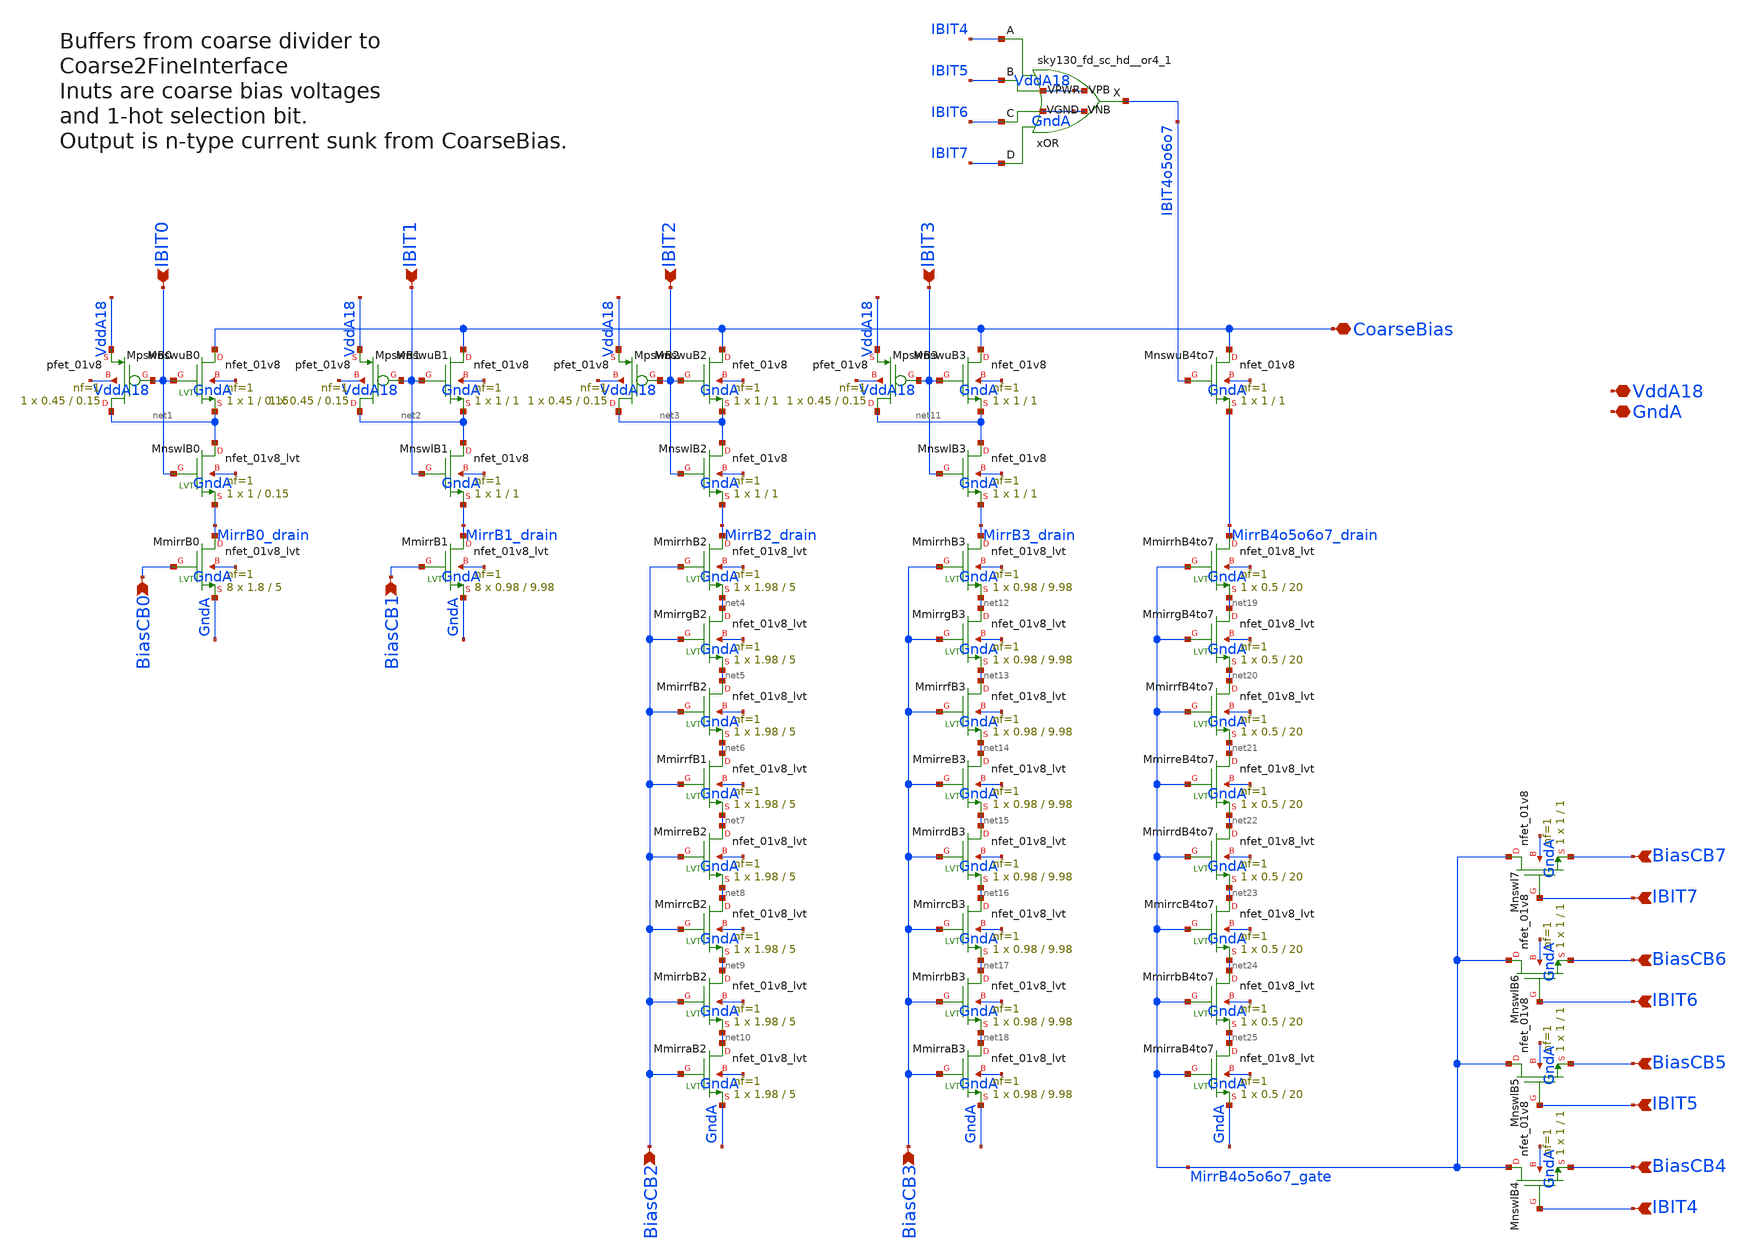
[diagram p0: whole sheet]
** sch_path: analog/xschem/BiasCoarseSel8to1.sch
**.subckt BiasCoarseSel8to1 IBIT0 BiasCB0 IBIT1 BiasCB1 IBIT2 BiasCB2 IBIT3 BiasCB3 BiasCB7 IBIT7
*+ BiasCB6 IBIT6 BiasCB5 IBIT5 BiasCB4 IBIT4 CoarseBias VddA18 GndA
*.ipin IBIT0
*.ipin BiasCB0
*.ipin IBIT1
*.ipin BiasCB1
*.ipin IBIT2
*.ipin BiasCB2
*.ipin IBIT3
*.ipin BiasCB3
*.ipin BiasCB7
*.ipin IBIT7
*.ipin BiasCB6
*.ipin IBIT6
*.ipin BiasCB5
*.ipin IBIT5
*.ipin BiasCB4
*.ipin IBIT4
*.iopin CoarseBias
*.iopin VddA18
*.iopin GndA
XMpswB0 net1 IBIT0 VddA18 VddA18 sky130_fd_pr__pfet_01v8 L=0.15 W=0.45 nf=1 ad='int((1 + 1)/2) * 0.45 / 1 * 0.29'
+ as='int((1 + 2)/2) * 0.45 / 1 * 0.29' pd='2*int((1 + 1)/2) * (0.45 / 1 + 0.29)' ps='2*int((1 + 2)/2) * (0.45 / 1 + 0.29)'
+ nrd='0.29 / 0.45 ' nrs='0.29 / 0.45 ' sa=0 sb=0 sd=0 mult=1 m=1
XMnswuB0 CoarseBias IBIT0 net1 GndA sky130_fd_pr__nfet_01v8 L=0.15 W=1 nf=1 ad='int((1 + 1)/2) * 1 / 1 * 0.29'
+ as='int((1 + 2)/2) * 1 / 1 * 0.29' pd='2*int((1 + 1)/2) * (1 / 1 + 0.29)' ps='2*int((1 + 2)/2) * (1 / 1 + 0.29)'
+ nrd='0.29 / 1 ' nrs='0.29 / 1 ' sa=0 sb=0 sd=0 mult=1 m=1
XMnswlB0 net1 IBIT0 MirrB0_drain GndA sky130_fd_pr__nfet_01v8_lvt L=0.15 W=1 nf=1 ad='int((1 + 1)/2) * 1 / 1 * 0.29'
+ as='int((1 + 2)/2) * 1 / 1 * 0.29' pd='2*int((1 + 1)/2) * (1 / 1 + 0.29)' ps='2*int((1 + 2)/2) * (1 / 1 + 0.29)'
+ nrd='0.29 / 1 ' nrs='0.29 / 1 ' sa=0 sb=0 sd=0 mult=1 m=1
XMmirrB0 MirrB0_drain BiasCB0 GndA GndA sky130_fd_pr__nfet_01v8_lvt L=5 W=1.8 nf=1 ad='int((1 + 1)/2) * 1.8 / 1 * 0.29'
+ as='int((1 + 2)/2) * 1.8 / 1 * 0.29' pd='2*int((1 + 1)/2) * (1.8 / 1 + 0.29)' ps='2*int((1 + 2)/2) * (1.8 / 1 + 0.29)'
+ nrd='0.29 / 1.8 ' nrs='0.29 / 1.8 ' sa=0 sb=0 sd=0 mult=8 m=8
XMpswB1 net2 IBIT1 VddA18 VddA18 sky130_fd_pr__pfet_01v8 L=0.15 W=0.45 nf=1 ad='int((1 + 1)/2) * 0.45 / 1 * 0.29'
+ as='int((1 + 2)/2) * 0.45 / 1 * 0.29' pd='2*int((1 + 1)/2) * (0.45 / 1 + 0.29)' ps='2*int((1 + 2)/2) * (0.45 / 1 + 0.29)'
+ nrd='0.29 / 0.45 ' nrs='0.29 / 0.45 ' sa=0 sb=0 sd=0 mult=1 m=1
XMnswuB1 CoarseBias IBIT1 net2 GndA sky130_fd_pr__nfet_01v8 L=1 W=1 nf=1 ad='int((1 + 1)/2) * 1 / 1 * 0.29'
+ as='int((1 + 2)/2) * 1 / 1 * 0.29' pd='2*int((1 + 1)/2) * (1 / 1 + 0.29)' ps='2*int((1 + 2)/2) * (1 / 1 + 0.29)'
+ nrd='0.29 / 1 ' nrs='0.29 / 1 ' sa=0 sb=0 sd=0 mult=1 m=1
XMnswlB1 net2 IBIT1 MirrB1_drain GndA sky130_fd_pr__nfet_01v8 L=1 W=1 nf=1 ad='int((1 + 1)/2) * 1 / 1 * 0.29'
+ as='int((1 + 2)/2) * 1 / 1 * 0.29' pd='2*int((1 + 1)/2) * (1 / 1 + 0.29)' ps='2*int((1 + 2)/2) * (1 / 1 + 0.29)'
+ nrd='0.29 / 1 ' nrs='0.29 / 1 ' sa=0 sb=0 sd=0 mult=1 m=1
XMmirrB1 MirrB1_drain BiasCB1 GndA GndA sky130_fd_pr__nfet_01v8_lvt L=9.98 W=0.98 nf=1 ad='int((1 + 1)/2) * 0.98 / 1 * 0.29'
+ as='int((1 + 2)/2) * 0.98 / 1 * 0.29' pd='2*int((1 + 1)/2) * (0.98 / 1 + 0.29)' ps='2*int((1 + 2)/2) * (0.98 / 1 + 0.29)'
+ nrd='0.29 / 0.98 ' nrs='0.29 / 0.98 ' sa=0 sb=0 sd=0 mult=8 m=8
XMpswB2 net3 IBIT2 VddA18 VddA18 sky130_fd_pr__pfet_01v8 L=0.15 W=0.45 nf=1 ad='int((1 + 1)/2) * 0.45 / 1 * 0.29'
+ as='int((1 + 2)/2) * 0.45 / 1 * 0.29' pd='2*int((1 + 1)/2) * (0.45 / 1 + 0.29)' ps='2*int((1 + 2)/2) * (0.45 / 1 + 0.29)'
+ nrd='0.29 / 0.45 ' nrs='0.29 / 0.45 ' sa=0 sb=0 sd=0 mult=1 m=1
XMnswuB2 CoarseBias IBIT2 net3 GndA sky130_fd_pr__nfet_01v8 L=1 W=1 nf=1 ad='int((1 + 1)/2) * 1 / 1 * 0.29'
+ as='int((1 + 2)/2) * 1 / 1 * 0.29' pd='2*int((1 + 1)/2) * (1 / 1 + 0.29)' ps='2*int((1 + 2)/2) * (1 / 1 + 0.29)'
+ nrd='0.29 / 1 ' nrs='0.29 / 1 ' sa=0 sb=0 sd=0 mult=1 m=1
XMnswlB2 net3 IBIT2 MirrB2_drain GndA sky130_fd_pr__nfet_01v8 L=1 W=1 nf=1 ad='int((1 + 1)/2) * 1 / 1 * 0.29'
+ as='int((1 + 2)/2) * 1 / 1 * 0.29' pd='2*int((1 + 1)/2) * (1 / 1 + 0.29)' ps='2*int((1 + 2)/2) * (1 / 1 + 0.29)'
+ nrd='0.29 / 1 ' nrs='0.29 / 1 ' sa=0 sb=0 sd=0 mult=1 m=1
XMmirrhB2 MirrB2_drain BiasCB2 net4 GndA sky130_fd_pr__nfet_01v8_lvt L=5 W=1.98 nf=1 ad='int((1 + 1)/2) * 1.98 / 1 * 0.29'
+ as='int((1 + 2)/2) * 1.98 / 1 * 0.29' pd='2*int((1 + 1)/2) * (1.98 / 1 + 0.29)' ps='2*int((1 + 2)/2) * (1.98 / 1 + 0.29)'
+ nrd='0.29 / 1.98 ' nrs='0.29 / 1.98 ' sa=0 sb=0 sd=0 mult=1 m=1
XMmirrgB2 net4 BiasCB2 net5 GndA sky130_fd_pr__nfet_01v8_lvt L=5 W=1.98 nf=1 ad='int((1 + 1)/2) * 1.98 / 1 * 0.29'
+ as='int((1 + 2)/2) * 1.98 / 1 * 0.29' pd='2*int((1 + 1)/2) * (1.98 / 1 + 0.29)' ps='2*int((1 + 2)/2) * (1.98 / 1 + 0.29)'
+ nrd='0.29 / 1.98 ' nrs='0.29 / 1.98 ' sa=0 sb=0 sd=0 mult=1 m=1
XMmirrfB2 net5 BiasCB2 net6 GndA sky130_fd_pr__nfet_01v8_lvt L=5 W=1.98 nf=1 ad='int((1 + 1)/2) * 1.98 / 1 * 0.29'
+ as='int((1 + 2)/2) * 1.98 / 1 * 0.29' pd='2*int((1 + 1)/2) * (1.98 / 1 + 0.29)' ps='2*int((1 + 2)/2) * (1.98 / 1 + 0.29)'
+ nrd='0.29 / 1.98 ' nrs='0.29 / 1.98 ' sa=0 sb=0 sd=0 mult=1 m=1
XMmirrfB1 net6 BiasCB2 net7 GndA sky130_fd_pr__nfet_01v8_lvt L=5 W=1.98 nf=1 ad='int((1 + 1)/2) * 1.98 / 1 * 0.29'
+ as='int((1 + 2)/2) * 1.98 / 1 * 0.29' pd='2*int((1 + 1)/2) * (1.98 / 1 + 0.29)' ps='2*int((1 + 2)/2) * (1.98 / 1 + 0.29)'
+ nrd='0.29 / 1.98 ' nrs='0.29 / 1.98 ' sa=0 sb=0 sd=0 mult=1 m=1
XMmirreB2 net7 BiasCB2 net8 GndA sky130_fd_pr__nfet_01v8_lvt L=5 W=1.98 nf=1 ad='int((1 + 1)/2) * 1.98 / 1 * 0.29'
+ as='int((1 + 2)/2) * 1.98 / 1 * 0.29' pd='2*int((1 + 1)/2) * (1.98 / 1 + 0.29)' ps='2*int((1 + 2)/2) * (1.98 / 1 + 0.29)'
+ nrd='0.29 / 1.98 ' nrs='0.29 / 1.98 ' sa=0 sb=0 sd=0 mult=1 m=1
XMmirrcB2 net8 BiasCB2 net9 GndA sky130_fd_pr__nfet_01v8_lvt L=5 W=1.98 nf=1 ad='int((1 + 1)/2) * 1.98 / 1 * 0.29'
+ as='int((1 + 2)/2) * 1.98 / 1 * 0.29' pd='2*int((1 + 1)/2) * (1.98 / 1 + 0.29)' ps='2*int((1 + 2)/2) * (1.98 / 1 + 0.29)'
+ nrd='0.29 / 1.98 ' nrs='0.29 / 1.98 ' sa=0 sb=0 sd=0 mult=1 m=1
XMmirrbB2 net9 BiasCB2 net10 GndA sky130_fd_pr__nfet_01v8_lvt L=5 W=1.98 nf=1 ad='int((1 + 1)/2) * 1.98 / 1 * 0.29'
+ as='int((1 + 2)/2) * 1.98 / 1 * 0.29' pd='2*int((1 + 1)/2) * (1.98 / 1 + 0.29)' ps='2*int((1 + 2)/2) * (1.98 / 1 + 0.29)'
+ nrd='0.29 / 1.98 ' nrs='0.29 / 1.98 ' sa=0 sb=0 sd=0 mult=1 m=1
XMmirraB2 net10 BiasCB2 GndA GndA sky130_fd_pr__nfet_01v8_lvt L=5 W=1.98 nf=1 ad='int((1 + 1)/2) * 1.98 / 1 * 0.29'
+ as='int((1 + 2)/2) * 1.98 / 1 * 0.29' pd='2*int((1 + 1)/2) * (1.98 / 1 + 0.29)' ps='2*int((1 + 2)/2) * (1.98 / 1 + 0.29)'
+ nrd='0.29 / 1.98 ' nrs='0.29 / 1.98 ' sa=0 sb=0 sd=0 mult=1 m=1
XMpswB3 net11 IBIT3 VddA18 VddA18 sky130_fd_pr__pfet_01v8 L=0.15 W=0.45 nf=1 ad='int((1 + 1)/2) * 0.45 / 1 * 0.29'
+ as='int((1 + 2)/2) * 0.45 / 1 * 0.29' pd='2*int((1 + 1)/2) * (0.45 / 1 + 0.29)' ps='2*int((1 + 2)/2) * (0.45 / 1 + 0.29)'
+ nrd='0.29 / 0.45 ' nrs='0.29 / 0.45 ' sa=0 sb=0 sd=0 mult=1 m=1
XMnswuB3 CoarseBias IBIT3 net11 GndA sky130_fd_pr__nfet_01v8 L=1 W=1 nf=1 ad='int((1 + 1)/2) * 1 / 1 * 0.29'
+ as='int((1 + 2)/2) * 1 / 1 * 0.29' pd='2*int((1 + 1)/2) * (1 / 1 + 0.29)' ps='2*int((1 + 2)/2) * (1 / 1 + 0.29)'
+ nrd='0.29 / 1 ' nrs='0.29 / 1 ' sa=0 sb=0 sd=0 mult=1 m=1
XMnswlB3 net11 IBIT3 MirrB3_drain GndA sky130_fd_pr__nfet_01v8 L=1 W=1 nf=1 ad='int((1 + 1)/2) * 1 / 1 * 0.29'
+ as='int((1 + 2)/2) * 1 / 1 * 0.29' pd='2*int((1 + 1)/2) * (1 / 1 + 0.29)' ps='2*int((1 + 2)/2) * (1 / 1 + 0.29)'
+ nrd='0.29 / 1 ' nrs='0.29 / 1 ' sa=0 sb=0 sd=0 mult=1 m=1
XMmirrhB3 MirrB3_drain BiasCB3 net12 GndA sky130_fd_pr__nfet_01v8_lvt L=9.98 W=0.98 nf=1 ad='int((1 + 1)/2) * 0.98 / 1 * 0.29'
+ as='int((1 + 2)/2) * 0.98 / 1 * 0.29' pd='2*int((1 + 1)/2) * (0.98 / 1 + 0.29)' ps='2*int((1 + 2)/2) * (0.98 / 1 + 0.29)'
+ nrd='0.29 / 0.98 ' nrs='0.29 / 0.98 ' sa=0 sb=0 sd=0 mult=1 m=1
XMmirrgB3 net12 BiasCB3 net13 GndA sky130_fd_pr__nfet_01v8_lvt L=9.98 W=0.98 nf=1 ad='int((1 + 1)/2) * 0.98 / 1 * 0.29'
+ as='int((1 + 2)/2) * 0.98 / 1 * 0.29' pd='2*int((1 + 1)/2) * (0.98 / 1 + 0.29)' ps='2*int((1 + 2)/2) * (0.98 / 1 + 0.29)'
+ nrd='0.29 / 0.98 ' nrs='0.29 / 0.98 ' sa=0 sb=0 sd=0 mult=1 m=1
XMmirrfB3 net13 BiasCB3 net14 GndA sky130_fd_pr__nfet_01v8_lvt L=9.98 W=0.98 nf=1 ad='int((1 + 1)/2) * 0.98 / 1 * 0.29'
+ as='int((1 + 2)/2) * 0.98 / 1 * 0.29' pd='2*int((1 + 1)/2) * (0.98 / 1 + 0.29)' ps='2*int((1 + 2)/2) * (0.98 / 1 + 0.29)'
+ nrd='0.29 / 0.98 ' nrs='0.29 / 0.98 ' sa=0 sb=0 sd=0 mult=1 m=1
XMmirreB3 net14 BiasCB3 net15 GndA sky130_fd_pr__nfet_01v8_lvt L=9.98 W=0.98 nf=1 ad='int((1 + 1)/2) * 0.98 / 1 * 0.29'
+ as='int((1 + 2)/2) * 0.98 / 1 * 0.29' pd='2*int((1 + 1)/2) * (0.98 / 1 + 0.29)' ps='2*int((1 + 2)/2) * (0.98 / 1 + 0.29)'
+ nrd='0.29 / 0.98 ' nrs='0.29 / 0.98 ' sa=0 sb=0 sd=0 mult=1 m=1
XMmirrdB3 net15 BiasCB3 net16 GndA sky130_fd_pr__nfet_01v8_lvt L=9.98 W=0.98 nf=1 ad='int((1 + 1)/2) * 0.98 / 1 * 0.29'
+ as='int((1 + 2)/2) * 0.98 / 1 * 0.29' pd='2*int((1 + 1)/2) * (0.98 / 1 + 0.29)' ps='2*int((1 + 2)/2) * (0.98 / 1 + 0.29)'
+ nrd='0.29 / 0.98 ' nrs='0.29 / 0.98 ' sa=0 sb=0 sd=0 mult=1 m=1
XMmirrcB3 net16 BiasCB3 net17 GndA sky130_fd_pr__nfet_01v8_lvt L=9.98 W=0.98 nf=1 ad='int((1 + 1)/2) * 0.98 / 1 * 0.29'
+ as='int((1 + 2)/2) * 0.98 / 1 * 0.29' pd='2*int((1 + 1)/2) * (0.98 / 1 + 0.29)' ps='2*int((1 + 2)/2) * (0.98 / 1 + 0.29)'
+ nrd='0.29 / 0.98 ' nrs='0.29 / 0.98 ' sa=0 sb=0 sd=0 mult=1 m=1
XMmirrbB3 net17 BiasCB3 net18 GndA sky130_fd_pr__nfet_01v8_lvt L=9.98 W=0.98 nf=1 ad='int((1 + 1)/2) * 0.98 / 1 * 0.29'
+ as='int((1 + 2)/2) * 0.98 / 1 * 0.29' pd='2*int((1 + 1)/2) * (0.98 / 1 + 0.29)' ps='2*int((1 + 2)/2) * (0.98 / 1 + 0.29)'
+ nrd='0.29 / 0.98 ' nrs='0.29 / 0.98 ' sa=0 sb=0 sd=0 mult=1 m=1
XMmirraB3 net18 BiasCB3 GndA GndA sky130_fd_pr__nfet_01v8_lvt L=9.98 W=0.98 nf=1 ad='int((1 + 1)/2) * 0.98 / 1 * 0.29'
+ as='int((1 + 2)/2) * 0.98 / 1 * 0.29' pd='2*int((1 + 1)/2) * (0.98 / 1 + 0.29)' ps='2*int((1 + 2)/2) * (0.98 / 1 + 0.29)'
+ nrd='0.29 / 0.98 ' nrs='0.29 / 0.98 ' sa=0 sb=0 sd=0 mult=1 m=1
XMnswuB4to7 CoarseBias IBIT4o5o6o7 MirrB4o5o6o7_drain GndA sky130_fd_pr__nfet_01v8 L=1 W=1 nf=1 ad='int((1 + 1)/2) * 1 / 1 * 0.29'
+ as='int((1 + 2)/2) * 1 / 1 * 0.29' pd='2*int((1 + 1)/2) * (1 / 1 + 0.29)' ps='2*int((1 + 2)/2) * (1 / 1 + 0.29)'
+ nrd='0.29 / 1 ' nrs='0.29 / 1 ' sa=0 sb=0 sd=0 mult=1 m=1
XMmirrhB4to7 MirrB4o5o6o7_drain MirrB4o5o6o7_gate net19 GndA sky130_fd_pr__nfet_01v8_lvt L=20 W=0.5 nf=1
+ ad='int((1 + 1)/2) * 0.5 / 1 * 0.29' as='int((1 + 2)/2) * 0.5 / 1 * 0.29' pd='2*int((1 + 1)/2) * (0.5 / 1 + 0.29)'
+ ps='2*int((1 + 2)/2) * (0.5 / 1 + 0.29)' nrd='0.29 / 0.5 ' nrs='0.29 / 0.5 ' sa=0 sb=0 sd=0 mult=1 m=1
XMmirraB4to7 net25 MirrB4o5o6o7_gate GndA GndA sky130_fd_pr__nfet_01v8_lvt L=20 W=0.5 nf=1 ad='int((1 + 1)/2) * 0.5 / 1 * 0.29'
+ as='int((1 + 2)/2) * 0.5 / 1 * 0.29' pd='2*int((1 + 1)/2) * (0.5 / 1 + 0.29)' ps='2*int((1 + 2)/2) * (0.5 / 1 + 0.29)'
+ nrd='0.29 / 0.5 ' nrs='0.29 / 0.5 ' sa=0 sb=0 sd=0 mult=1 m=1
XMmirrbB4to7 net24 MirrB4o5o6o7_gate net25 GndA sky130_fd_pr__nfet_01v8_lvt L=20 W=0.5 nf=1 ad='int((1 + 1)/2) * 0.5 / 1 * 0.29'
+ as='int((1 + 2)/2) * 0.5 / 1 * 0.29' pd='2*int((1 + 1)/2) * (0.5 / 1 + 0.29)' ps='2*int((1 + 2)/2) * (0.5 / 1 + 0.29)'
+ nrd='0.29 / 0.5 ' nrs='0.29 / 0.5 ' sa=0 sb=0 sd=0 mult=1 m=1
XMmirrcB4to7 net23 MirrB4o5o6o7_gate net24 GndA sky130_fd_pr__nfet_01v8_lvt L=20 W=0.5 nf=1 ad='int((1 + 1)/2) * 0.5 / 1 * 0.29'
+ as='int((1 + 2)/2) * 0.5 / 1 * 0.29' pd='2*int((1 + 1)/2) * (0.5 / 1 + 0.29)' ps='2*int((1 + 2)/2) * (0.5 / 1 + 0.29)'
+ nrd='0.29 / 0.5 ' nrs='0.29 / 0.5 ' sa=0 sb=0 sd=0 mult=1 m=1
XMmirrdB4to7 net22 MirrB4o5o6o7_gate net23 GndA sky130_fd_pr__nfet_01v8_lvt L=20 W=0.5 nf=1 ad='int((1 + 1)/2) * 0.5 / 1 * 0.29'
+ as='int((1 + 2)/2) * 0.5 / 1 * 0.29' pd='2*int((1 + 1)/2) * (0.5 / 1 + 0.29)' ps='2*int((1 + 2)/2) * (0.5 / 1 + 0.29)'
+ nrd='0.29 / 0.5 ' nrs='0.29 / 0.5 ' sa=0 sb=0 sd=0 mult=1 m=1
XMmirreB4to7 net21 MirrB4o5o6o7_gate net22 GndA sky130_fd_pr__nfet_01v8_lvt L=20 W=0.5 nf=1 ad='int((1 + 1)/2) * 0.5 / 1 * 0.29'
+ as='int((1 + 2)/2) * 0.5 / 1 * 0.29' pd='2*int((1 + 1)/2) * (0.5 / 1 + 0.29)' ps='2*int((1 + 2)/2) * (0.5 / 1 + 0.29)'
+ nrd='0.29 / 0.5 ' nrs='0.29 / 0.5 ' sa=0 sb=0 sd=0 mult=1 m=1
XMmirrfB4to7 net20 MirrB4o5o6o7_gate net21 GndA sky130_fd_pr__nfet_01v8_lvt L=20 W=0.5 nf=1 ad='int((1 + 1)/2) * 0.5 / 1 * 0.29'
+ as='int((1 + 2)/2) * 0.5 / 1 * 0.29' pd='2*int((1 + 1)/2) * (0.5 / 1 + 0.29)' ps='2*int((1 + 2)/2) * (0.5 / 1 + 0.29)'
+ nrd='0.29 / 0.5 ' nrs='0.29 / 0.5 ' sa=0 sb=0 sd=0 mult=1 m=1
XMmirrgB4to7 net19 MirrB4o5o6o7_gate net20 GndA sky130_fd_pr__nfet_01v8_lvt L=20 W=0.5 nf=1 ad='int((1 + 1)/2) * 0.5 / 1 * 0.29'
+ as='int((1 + 2)/2) * 0.5 / 1 * 0.29' pd='2*int((1 + 1)/2) * (0.5 / 1 + 0.29)' ps='2*int((1 + 2)/2) * (0.5 / 1 + 0.29)'
+ nrd='0.29 / 0.5 ' nrs='0.29 / 0.5 ' sa=0 sb=0 sd=0 mult=1 m=1
XMnswl7 MirrB4o5o6o7_gate IBIT7 BiasCB7 GndA sky130_fd_pr__nfet_01v8 L=1 W=1 nf=1 ad='int((1 + 1)/2) * 1 / 1 * 0.29'
+ as='int((1 + 2)/2) * 1 / 1 * 0.29' pd='2*int((1 + 1)/2) * (1 / 1 + 0.29)' ps='2*int((1 + 2)/2) * (1 / 1 + 0.29)'
+ nrd='0.29 / 1 ' nrs='0.29 / 1 ' sa=0 sb=0 sd=0 mult=1 m=1
XMnswlB6 MirrB4o5o6o7_gate IBIT6 BiasCB6 GndA sky130_fd_pr__nfet_01v8 L=1 W=1 nf=1 ad='int((1 + 1)/2) * 1 / 1 * 0.29'
+ as='int((1 + 2)/2) * 1 / 1 * 0.29' pd='2*int((1 + 1)/2) * (1 / 1 + 0.29)' ps='2*int((1 + 2)/2) * (1 / 1 + 0.29)'
+ nrd='0.29 / 1 ' nrs='0.29 / 1 ' sa=0 sb=0 sd=0 mult=1 m=1
XMnswlB5 MirrB4o5o6o7_gate IBIT5 BiasCB5 GndA sky130_fd_pr__nfet_01v8 L=1 W=1 nf=1 ad='int((1 + 1)/2) * 1 / 1 * 0.29'
+ as='int((1 + 2)/2) * 1 / 1 * 0.29' pd='2*int((1 + 1)/2) * (1 / 1 + 0.29)' ps='2*int((1 + 2)/2) * (1 / 1 + 0.29)'
+ nrd='0.29 / 1 ' nrs='0.29 / 1 ' sa=0 sb=0 sd=0 mult=1 m=1
XMnswlB4 MirrB4o5o6o7_gate IBIT4 BiasCB4 GndA sky130_fd_pr__nfet_01v8 L=1 W=1 nf=1 ad='int((1 + 1)/2) * 1 / 1 * 0.29'
+ as='int((1 + 2)/2) * 1 / 1 * 0.29' pd='2*int((1 + 1)/2) * (1 / 1 + 0.29)' ps='2*int((1 + 2)/2) * (1 / 1 + 0.29)'
+ nrd='0.29 / 1 ' nrs='0.29 / 1 ' sa=0 sb=0 sd=0 mult=1 m=1
xOR IBIT4 IBIT5 IBIT6 IBIT7 IBIT4o5o6o7 VddA18 VddA18 GndA GndA sky130_fd_sc_hd__or4_1
**.ends
.end
